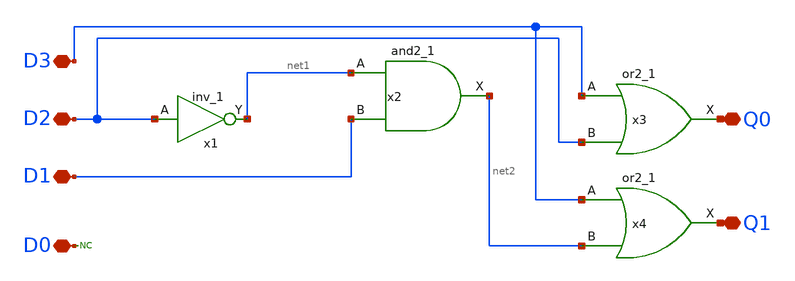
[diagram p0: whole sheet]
** sch_path: PriorityEncoder/2to4_Priority_Encoder_v0p0p1.sch
.lib $::SKYWATER_MODELS/sky130.lib.spice tt
.include $::SKYWATER_STDCELLS/sky130_fd_sc_hd.spice

**.subckt 2to4_Priority_Encoder_v0p0p1 D2 D1 D0 Q1 D3 Q0
*.iopin D2
*.iopin D1
*.iopin D0
*.iopin Q1
*.iopin D3
*.iopin Q0
x1 D2 GND GND VDD VDD net1 sky130_fd_sc_hd__inv_1
x2 net1 D1 GND GND VDD VDD net2 sky130_fd_sc_hd__and2_1
x3 D3 D2 GND GND VDD VDD Q0 sky130_fd_sc_hd__or2_1
x4 D3 net2 GND GND VDD VDD Q1 sky130_fd_sc_hd__or2_1
* noconn D0
**.ends
.end
